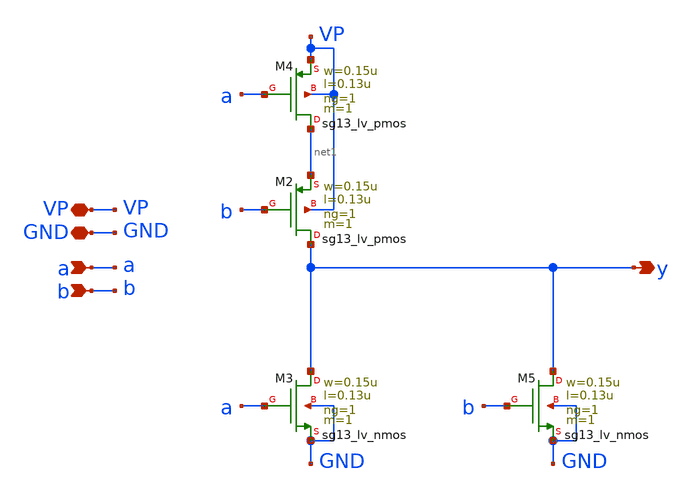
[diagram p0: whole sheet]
** sch_path: schematics/divider/schematics/NOR_2in.sch
**.subckt NOR_2in y GND a VP b
*.opin y
*.iopin GND
*.ipin a
*.iopin VP
*.ipin b
XM3 y a GND GND sg13_lv_nmos w=0.15u l=0.13u ng=1 m=1 mm_ok=1
XM2 y b net1 VP sg13_lv_pmos w=0.15u l=0.13u ng=1 m=1 mm_ok=1
XM4 net1 a VP VP sg13_lv_pmos w=0.15u l=0.13u ng=1 m=1 mm_ok=1
XM5 y b GND GND sg13_lv_nmos w=0.15u l=0.13u ng=1 m=1 mm_ok=1
**.ends
.end
